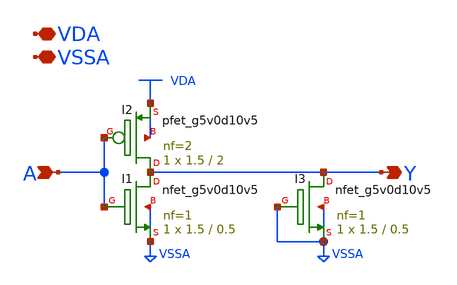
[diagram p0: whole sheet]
** sch_path: gpiov2_amx_pdcsd_inv.sch
* Copyright 2023 David Mitchell Bailey
* Licensed under the Apache License, Version 2.0 (the "License");
* you may not use this file except in compliance with the License.
* You may obtain a copy of the License at
* https://www.apache.org/licenses/LICENSE-2.0
* Unless required by applicable law or agreed to in writing, software
* distributed under the License is distributed on an "AS IS" BASIS,
* WITHOUT WARRANTIES OR CONDITIONS OF ANY KIND, either express or implied.
* See the License for the specific language governing permissions and
* limitations under the License.
**.subckt gpiov2_amx_pdcsd_inv A Y VDA VSSA
*.ipin A
*.opin Y
*.iopin VDA
*.iopin VSSA
XI1 Y A VSSA VSSA sky130_fd_pr__nfet_g5v0d10v5 L=0.5 W=1.5 nf=1 ad='int((nf+1)/2) * W/nf * 0.29' as='int((nf+2)/2) * W/nf * 0.29'
+ pd='2*int((nf+1)/2) * (W/nf + 0.29)' ps='2*int((nf+2)/2) * (W/nf + 0.29)' nrd='0.29 / W' nrs='0.29 / W'
+ sa=0 sb=0 sd=0 mult=1 m=1
XI2 Y A VDA VDA sky130_fd_pr__pfet_g5v0d10v5 L=2 W=1.5 nf=2 ad='int((nf+1)/2) * W/nf * 0.29' as='int((nf+2)/2) * W/nf * 0.29'
+ pd='2*int((nf+1)/2) * (W/nf + 0.29)' ps='2*int((nf+2)/2) * (W/nf + 0.29)' nrd='0.29 / W' nrs='0.29 / W'
+ sa=0 sb=0 sd=0 mult=1 m=1
XI3 Y VSSA VSSA VSSA sky130_fd_pr__nfet_g5v0d10v5 L=0.5 W=1.5 nf=1 ad='int((nf+1)/2) * W/nf * 0.29' as='int((nf+2)/2) * W/nf * 0.29'
+ pd='2*int((nf+1)/2) * (W/nf + 0.29)' ps='2*int((nf+2)/2) * (W/nf + 0.29)' nrd='0.29 / W' nrs='0.29 / W'
+ sa=0 sb=0 sd=0 mult=1 m=1
**.ends
.end
